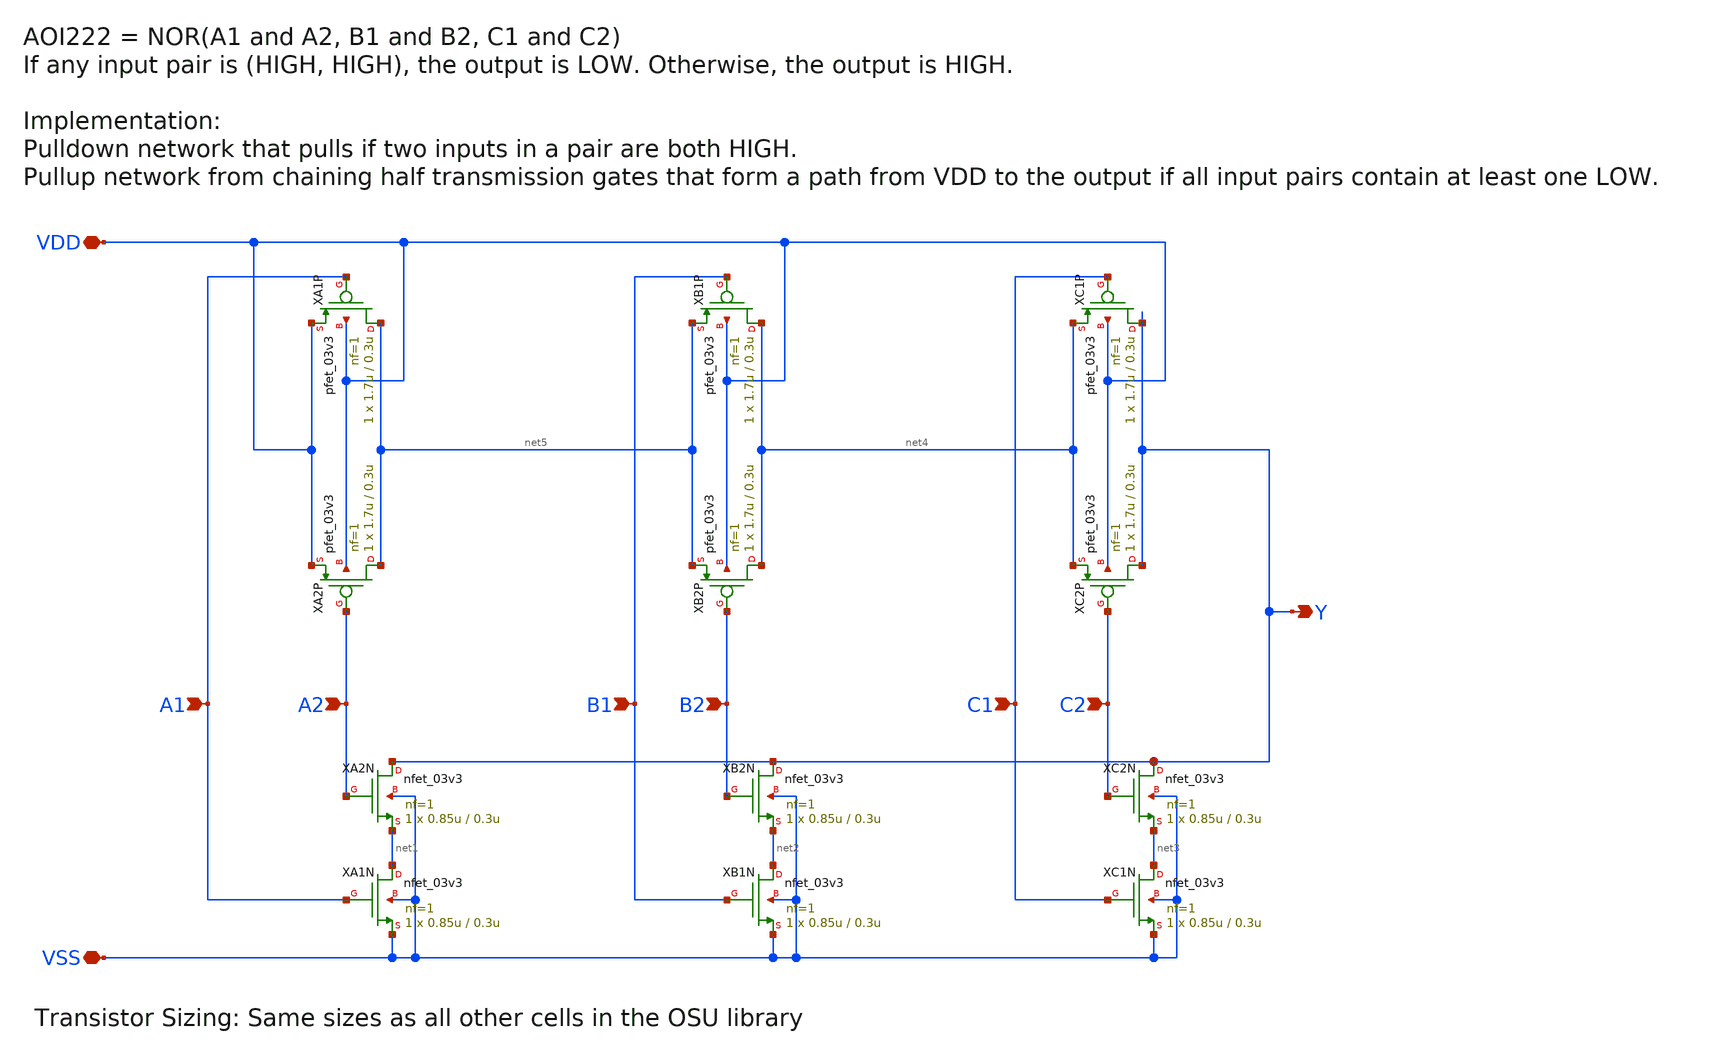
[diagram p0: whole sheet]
** sch_path: globalfoundries-pdk-libs-gf180mcu_sah_sc/cells/aoi222/gf180mcu_sah_sc_aoi222_1.sch
**.subckt gf180mcu_sah_sc_aoi222_1 A1 Y B1 C1 VDD B2 C2 A2 VSS
*.ipin A1
*.opin Y
*.ipin B1
*.ipin C1
*.iopin VDD
*.ipin B2
*.ipin C2
*.ipin A2
*.iopin VSS
XA2N Y A2 net1 VSS nfet_03v3 L=0.3u W=0.85u nf=1 ad='int((nf+1)/2) * W/nf * 0.18u' as='int((nf+2)/2) * W/nf * 0.18u'
+ pd='2*int((nf+1)/2) * (W/nf + 0.18u)' ps='2*int((nf+2)/2) * (W/nf + 0.18u)' nrd='0.18u / W' nrs='0.18u / W'
+ sa=0 sb=0 sd=0 m=1
XA1N net1 A1 VSS VSS nfet_03v3 L=0.3u W=0.85u nf=1 ad='int((nf+1)/2) * W/nf * 0.18u' as='int((nf+2)/2) * W/nf * 0.18u'
+ pd='2*int((nf+1)/2) * (W/nf + 0.18u)' ps='2*int((nf+2)/2) * (W/nf + 0.18u)' nrd='0.18u / W' nrs='0.18u / W'
+ sa=0 sb=0 sd=0 m=1
XA1P net5 A1 VDD VDD pfet_03v3 L=0.3u W=1.7u nf=1 ad='int((nf+1)/2) * W/nf * 0.18u' as='int((nf+2)/2) * W/nf * 0.18u'
+ pd='2*int((nf+1)/2) * (W/nf + 0.18u)' ps='2*int((nf+2)/2) * (W/nf + 0.18u)' nrd='0.18u / W' nrs='0.18u / W'
+ sa=0 sb=0 sd=0 m=1
XA2P net5 A2 VDD VDD pfet_03v3 L=0.3u W=1.7u nf=1 ad='int((nf+1)/2) * W/nf * 0.18u' as='int((nf+2)/2) * W/nf * 0.18u'
+ pd='2*int((nf+1)/2) * (W/nf + 0.18u)' ps='2*int((nf+2)/2) * (W/nf + 0.18u)' nrd='0.18u / W' nrs='0.18u / W'
+ sa=0 sb=0 sd=0 m=1
XB2N Y B2 net2 VSS nfet_03v3 L=0.3u W=0.85u nf=1 ad='int((nf+1)/2) * W/nf * 0.18u' as='int((nf+2)/2) * W/nf * 0.18u'
+ pd='2*int((nf+1)/2) * (W/nf + 0.18u)' ps='2*int((nf+2)/2) * (W/nf + 0.18u)' nrd='0.18u / W' nrs='0.18u / W'
+ sa=0 sb=0 sd=0 m=1
XB1N net2 B1 VSS VSS nfet_03v3 L=0.3u W=0.85u nf=1 ad='int((nf+1)/2) * W/nf * 0.18u' as='int((nf+2)/2) * W/nf * 0.18u'
+ pd='2*int((nf+1)/2) * (W/nf + 0.18u)' ps='2*int((nf+2)/2) * (W/nf + 0.18u)' nrd='0.18u / W' nrs='0.18u / W'
+ sa=0 sb=0 sd=0 m=1
XB1P net4 B1 net5 VDD pfet_03v3 L=0.3u W=1.7u nf=1 ad='int((nf+1)/2) * W/nf * 0.18u' as='int((nf+2)/2) * W/nf * 0.18u'
+ pd='2*int((nf+1)/2) * (W/nf + 0.18u)' ps='2*int((nf+2)/2) * (W/nf + 0.18u)' nrd='0.18u / W' nrs='0.18u / W'
+ sa=0 sb=0 sd=0 m=1
XB2P net4 B2 net5 VDD pfet_03v3 L=0.3u W=1.7u nf=1 ad='int((nf+1)/2) * W/nf * 0.18u' as='int((nf+2)/2) * W/nf * 0.18u'
+ pd='2*int((nf+1)/2) * (W/nf + 0.18u)' ps='2*int((nf+2)/2) * (W/nf + 0.18u)' nrd='0.18u / W' nrs='0.18u / W'
+ sa=0 sb=0 sd=0 m=1
XC2N Y C2 net3 VSS nfet_03v3 L=0.3u W=0.85u nf=1 ad='int((nf+1)/2) * W/nf * 0.18u' as='int((nf+2)/2) * W/nf * 0.18u'
+ pd='2*int((nf+1)/2) * (W/nf + 0.18u)' ps='2*int((nf+2)/2) * (W/nf + 0.18u)' nrd='0.18u / W' nrs='0.18u / W'
+ sa=0 sb=0 sd=0 m=1
XC1N net3 C1 VSS VSS nfet_03v3 L=0.3u W=0.85u nf=1 ad='int((nf+1)/2) * W/nf * 0.18u' as='int((nf+2)/2) * W/nf * 0.18u'
+ pd='2*int((nf+1)/2) * (W/nf + 0.18u)' ps='2*int((nf+2)/2) * (W/nf + 0.18u)' nrd='0.18u / W' nrs='0.18u / W'
+ sa=0 sb=0 sd=0 m=1
XC1P Y C1 net4 VDD pfet_03v3 L=0.3u W=1.7u nf=1 ad='int((nf+1)/2) * W/nf * 0.18u' as='int((nf+2)/2) * W/nf * 0.18u'
+ pd='2*int((nf+1)/2) * (W/nf + 0.18u)' ps='2*int((nf+2)/2) * (W/nf + 0.18u)' nrd='0.18u / W' nrs='0.18u / W'
+ sa=0 sb=0 sd=0 m=1
XC2P Y C2 net4 VDD pfet_03v3 L=0.3u W=1.7u nf=1 ad='int((nf+1)/2) * W/nf * 0.18u' as='int((nf+2)/2) * W/nf * 0.18u'
+ pd='2*int((nf+1)/2) * (W/nf + 0.18u)' ps='2*int((nf+2)/2) * (W/nf + 0.18u)' nrd='0.18u / W' nrs='0.18u / W'
+ sa=0 sb=0 sd=0 m=1
**.ends
.end
